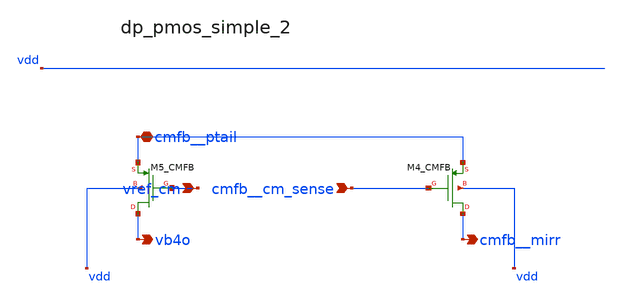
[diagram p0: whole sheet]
** sch_path: analog-db/raw/amp_034_fan_chopper_cmfb/hier/blocks/dp_pmos_simple_2.sch
**.subckt dp_pmos_simple_2 vref_cm cmfb__cm_sense cmfb__ptail vb4o cmfb__mirr
*.ipin vref_cm
*.ipin cmfb__cm_sense
*.iopin cmfb__ptail
*.opin vb4o
*.opin cmfb__mirr
XM4_CMFB cmfb__mirr cmfb__cm_sense cmfb__ptail vdd sg13_lv_pmos w=x_dut_xm4_cmfb_w
+ l=x_dut_xm4_cmfb_l ng=1 m=x_dut_xm4_cmfb_m
XM5_CMFB vb4o vref_cm cmfb__ptail vdd sg13_lv_pmos w=x_dut_xm5_cmfb_w l=x_dut_xm5_cmfb_l ng=1
+ m=x_dut_xm5_cmfb_m
**.ends
.end
